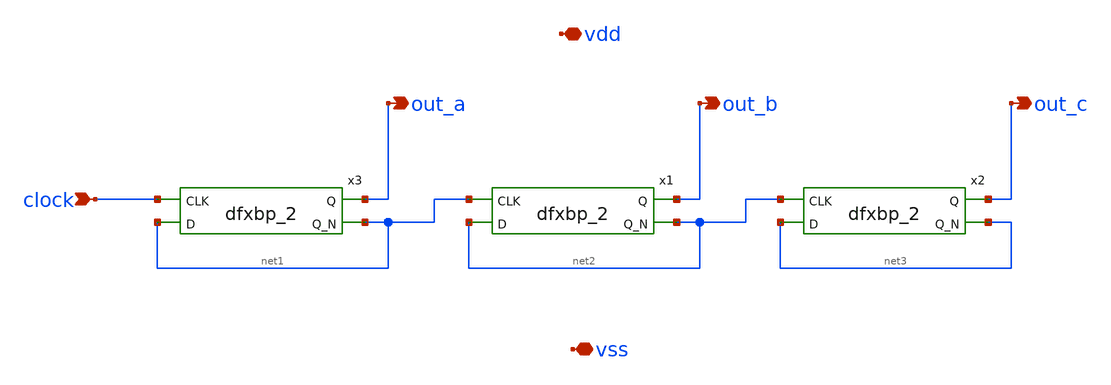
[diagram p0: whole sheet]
** sch_path: magic/divider/divider_3N.sch
**.subckt divider_3N clock out_a out_b out_c vdd vss
*.ipin clock
*.opin out_a
*.opin out_b
*.opin out_c
*.iopin vdd
*.iopin vss
x3 clock net1 VSS VSS VDD VDD out_a net1 sky130_fd_sc_hd__dfxbp_2
x1 net1 net2 VSS VSS VDD VDD out_b net2 sky130_fd_sc_hd__dfxbp_2
x2 net2 net3 VSS VSS VDD VDD out_c net3 sky130_fd_sc_hd__dfxbp_2
**.ends
.end
